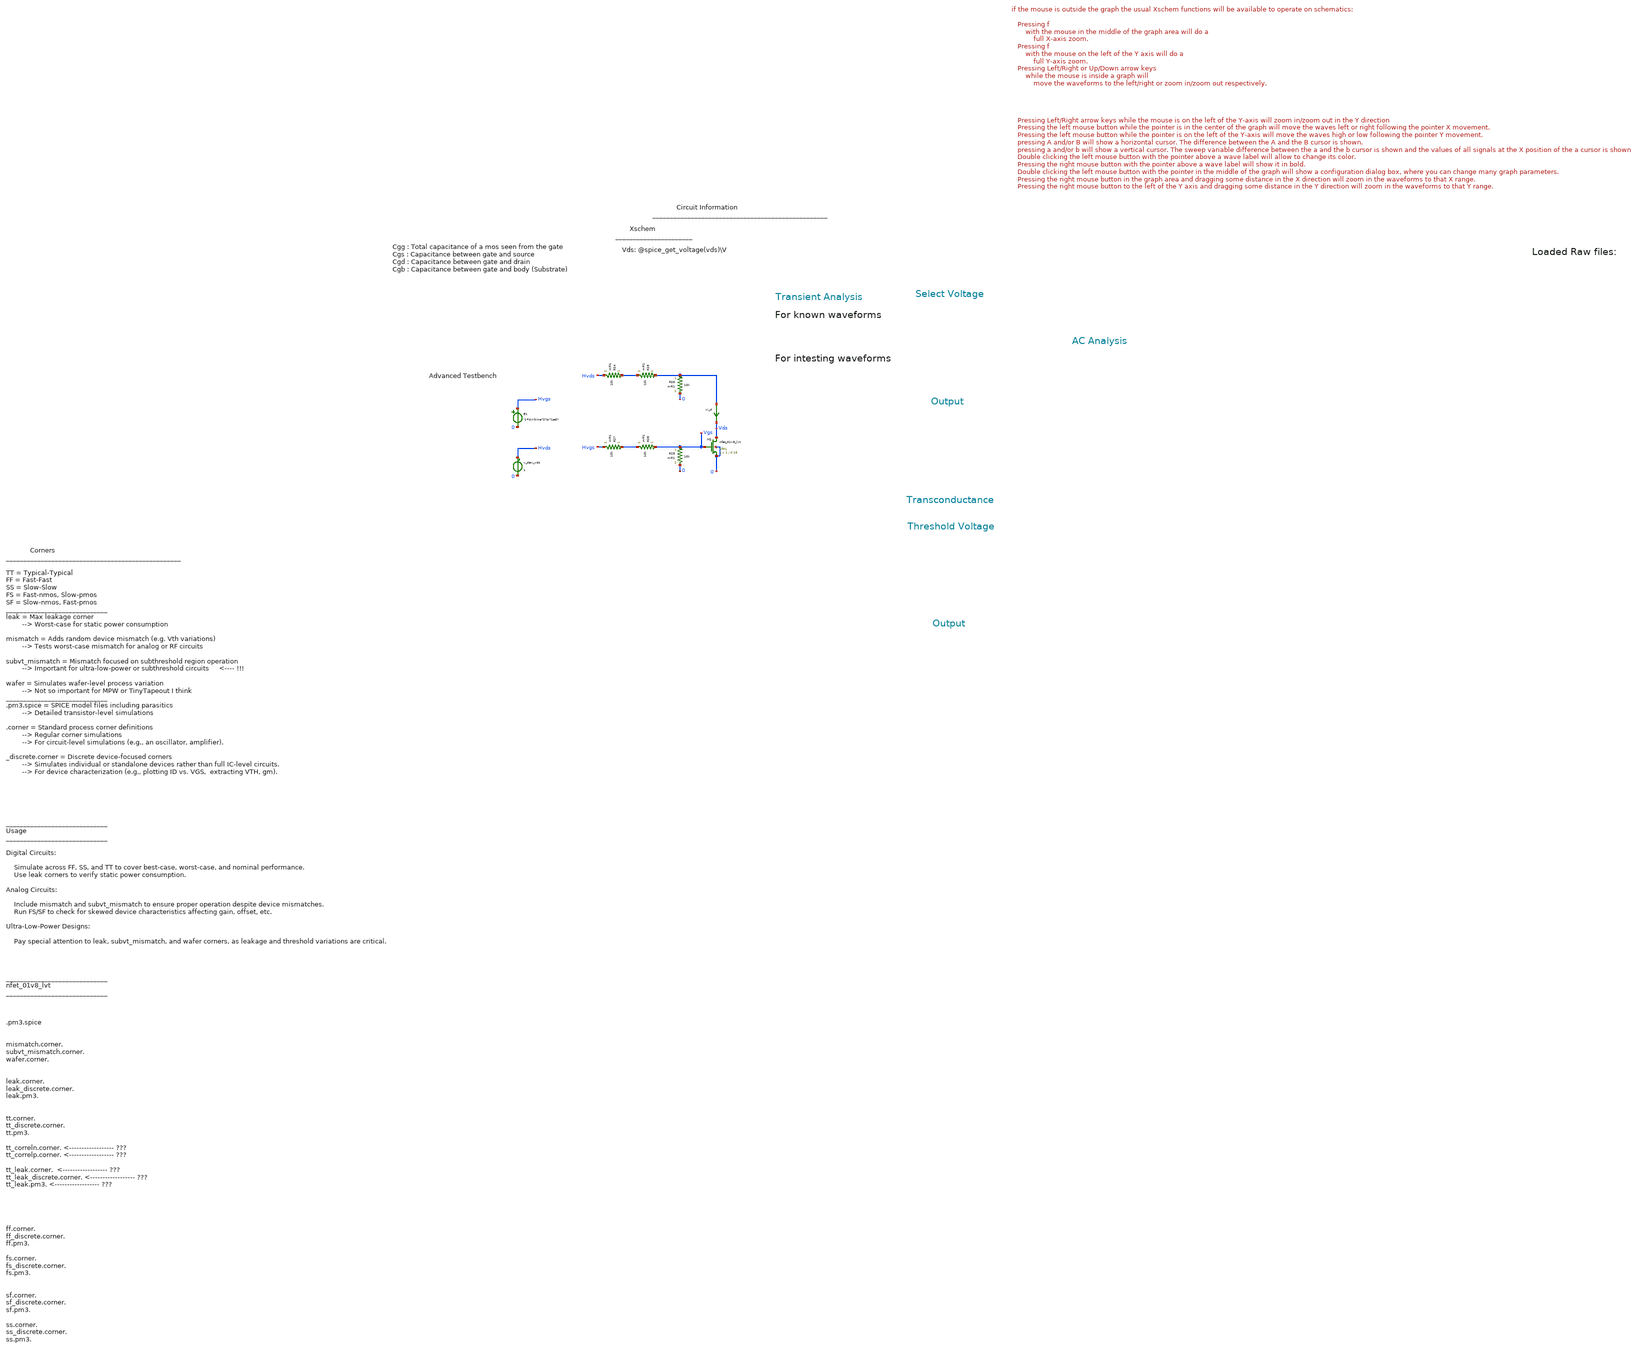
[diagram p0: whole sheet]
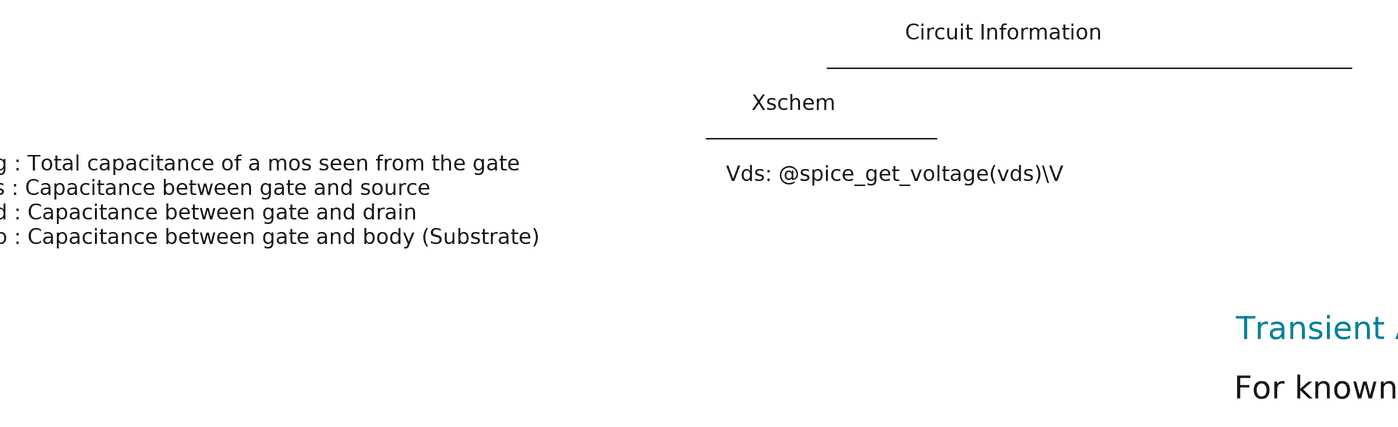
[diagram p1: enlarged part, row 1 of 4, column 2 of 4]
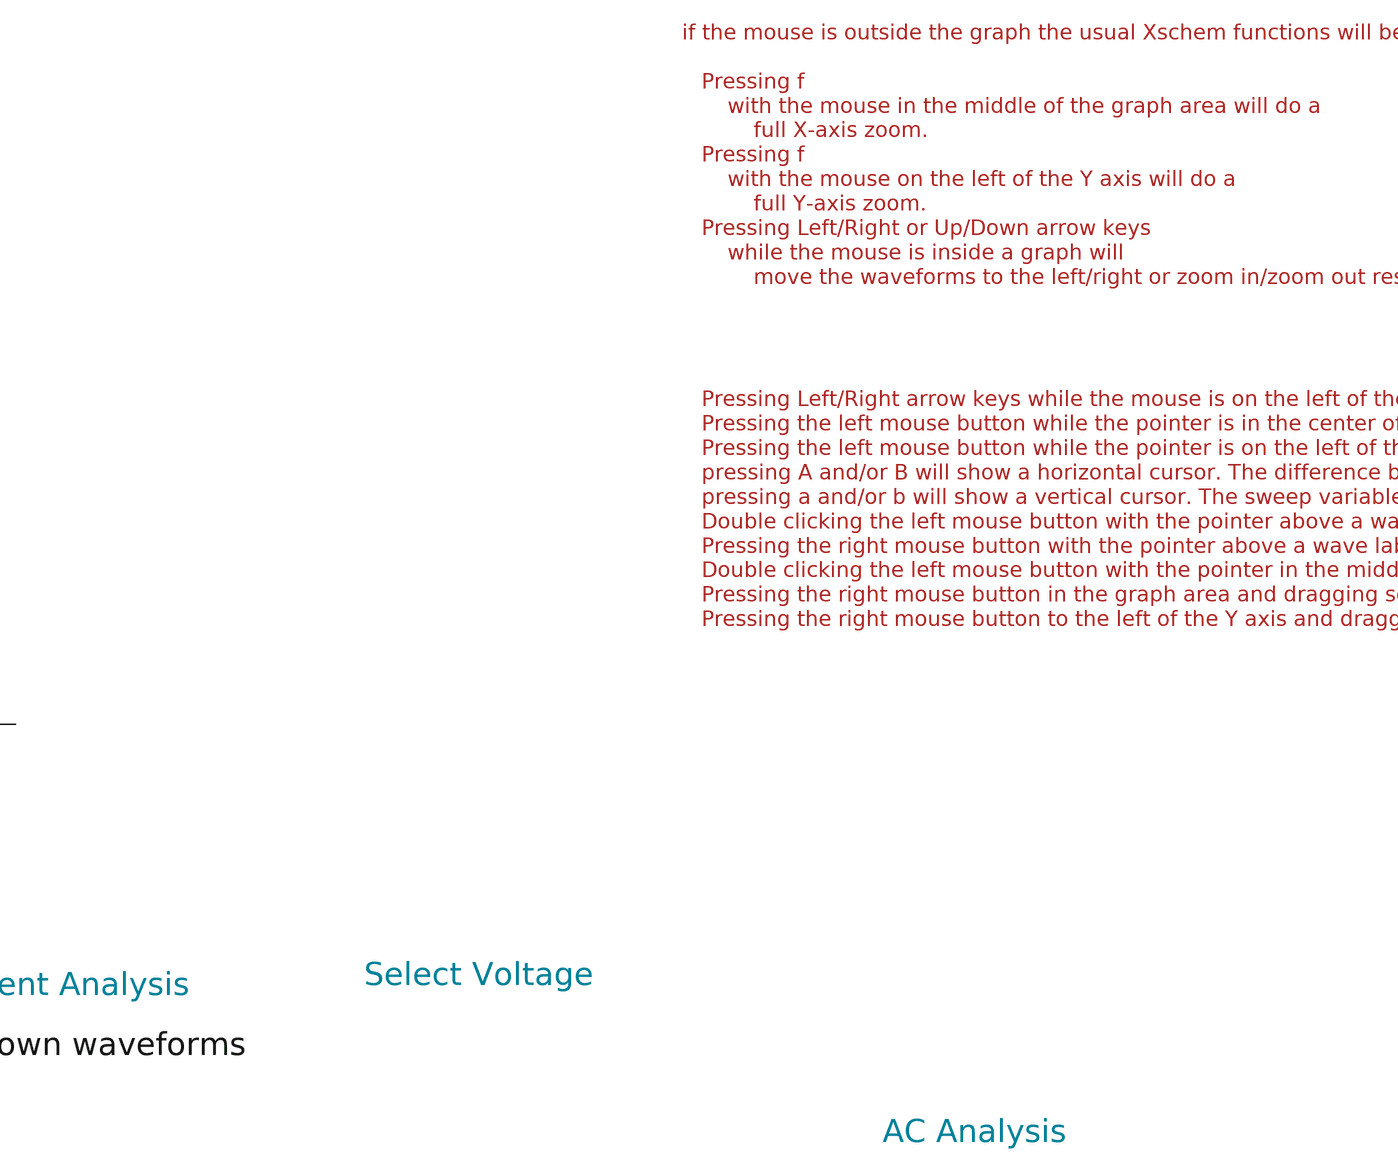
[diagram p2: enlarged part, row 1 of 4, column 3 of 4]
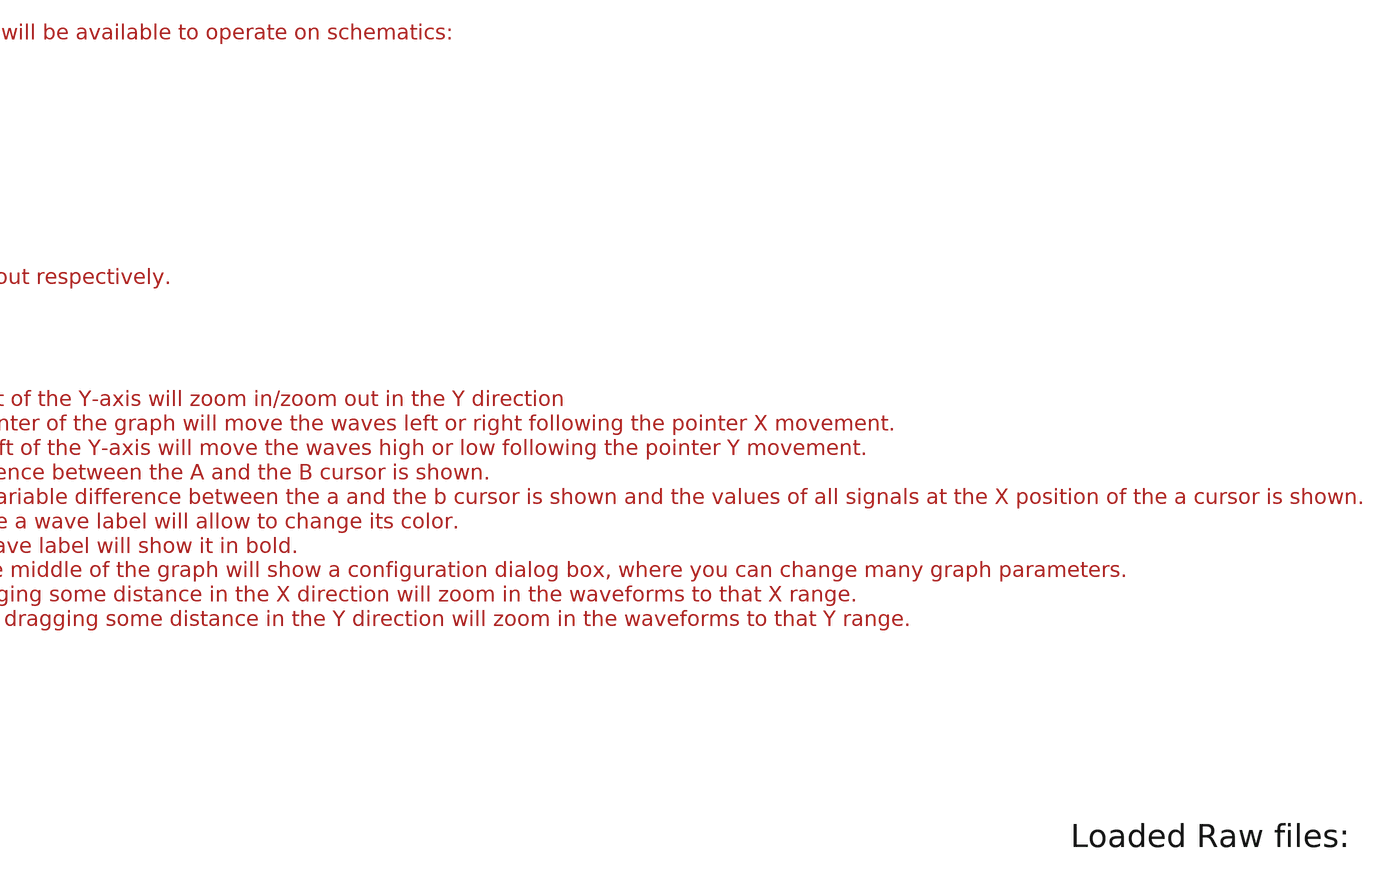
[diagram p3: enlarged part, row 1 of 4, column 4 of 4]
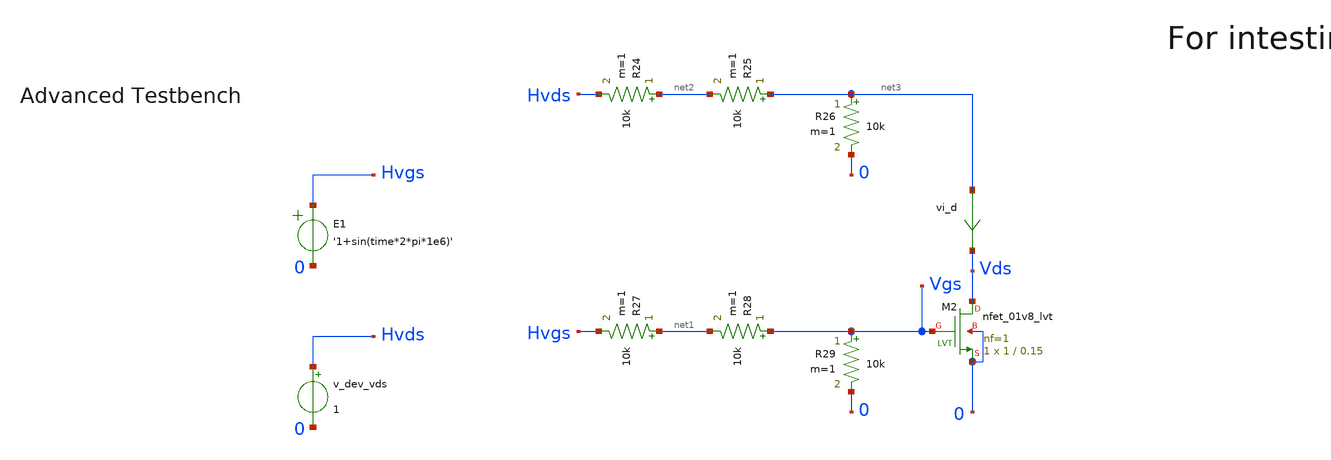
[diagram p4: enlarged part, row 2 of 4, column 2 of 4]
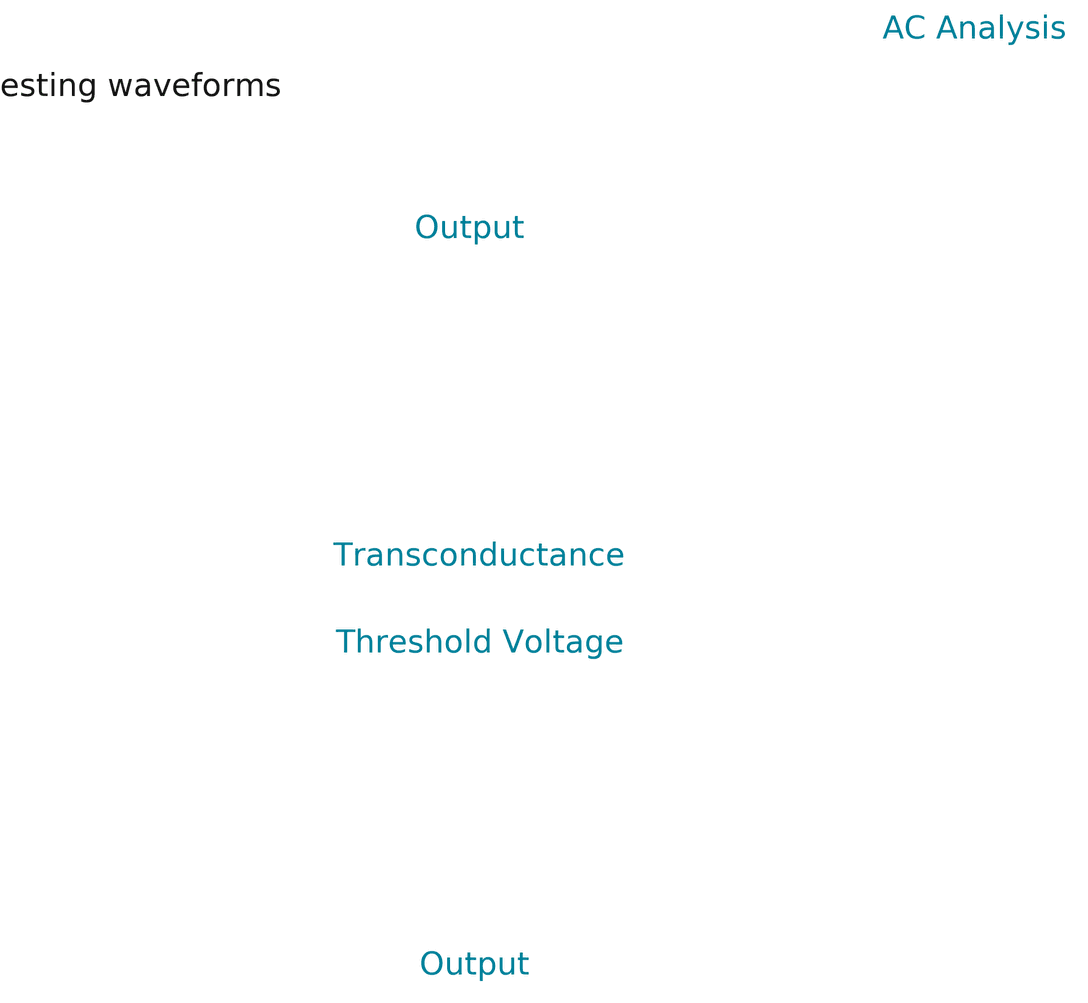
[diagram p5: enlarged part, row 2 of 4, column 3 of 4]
** sch_path: tt10-hdl/tt_um_test_commit/xschem/T0/nmos_tran.sch
* Copyright (C) 1998-2024 Stefan Frederik Schippers
* This program is free software; you can redistribute it and/or modify
* it under the terms of the GNU General Public License as published by
* the Free Software Foundation; either version 2 of the License, or
* (at your option) any later version.
* This program is distributed in the hope that it will be useful,
* but WITHOUT ANY WARRANTY; without even the implied warranty of
* MERCHANTABILITY or FITNESS FOR A PARTICULAR PURPOSE.  See the
* GNU General Public License for more details.
* You should have received a copy of the GNU General Public License
* along with this program; if not, write to the Free Software
**.subckt nmos_tran
vi_d net3 Vds 0
.save i(vi_d)
v_dev_vds Hvds 0 1
E1 Hvgs 0 VOL=' '1+sin(time*2*pi*1e6)' '
R27 net1 Hvgs 10k m=1
R28 Vgs net1 10k m=1
R29 Vgs 0 10k m=1
XM2 Vds Vgs 0 0 sky130_fd_pr__nfet_01v8_lvt L=0.15 W=1 nf=1 ad='int((1 + 1)/2) * 1 / 1 * 0.29' as='int((1 + 2)/2) * 1 / 1 * 0.29'
+ pd='2*int((1 + 1)/2) * (1 / 1 + 0.29)' ps='2*int((1 + 2)/2) * (1 / 1 + 0.29)' nrd='0.29 / 1 ' nrs='0.29 / 1 '
+ sa=0 sb=0 sd=0 mult=1 m=1
R24 net2 Hvds 10k m=1
R25 net3 net2 10k m=1
R26 net3 0 10k m=1
**** begin user architecture code



.temp 30

*.option gmin=5n
*.option scale=1e-6
.option wnflag=1
.option savecurrents

.save all
.control
  save all alli

  save @m.xm1.msky130_fd_pr__nfet_01v8_lvt[gm]
  save @m.xm1.msky130_fd_pr__nfet_01v8_lvt[id]
  save @m.xm1.msky130_fd_pr__nfet_01v8_lvt[vgs]

  save @m.xm1.msky130_fd_pr__nfet_01v8_lvt[cgg]
  save @m.xm1.msky130_fd_pr__nfet_01v8_lvt[cgs]
  save @m.xm1.msky130_fd_pr__nfet_01v8_lvt[cgdo]
  save @m.xm1.msky130_fd_pr__nfet_01v8_lvt[cgb]

  save @m.xm1.msky130_fd_pr__nfet_01v8_lvt[vds]
  save @m.xm1.msky130_fd_pr__nfet_01v8_lvt[vdsat]
  save @m.xm1.msky130_fd_pr__nfet_01v8_lvt[vth]


  save @m.xm1.msky130_fd_pr__nfet_01v8_lvt[leff]
  save @m.xm1.msky130_fd_pr__nfet_01v8_lvt[weff]
  save @m.xm1.msky130_fd_pr__nfet_01v8_lvt[gds]
  save @m.xm1.msky130_fd_pr__nfet_01v8_lvt[l]
  save @m.xm1.msky130_fd_pr__nfet_01v8_lvt[w]
  save @m.xm1.msky130_fd_pr__nfet_01v8_lvt[gm]
  save @m.xm1.msky130_fd_pr__nfet_01v8_lvt[gm]
  save @m.xm1.msky130_fd_pr__nfet_01v8_lvt[gm]
  save @m.xm1.msky130_fd_pr__nfet_01v8_lvt[gm]
  save @m.xm1.msky130_fd_pr__nfet_01v8_lvt[gm]



  *dc v_dev_vds 0 1.8 0.005 v_dev_vgs 0 1.8 0.2
  *write nmos_tb.raw




  tran 1n 5u
  write nmos_tb_tran.raw

  op
  set appendwrite
  write nmos_tb_tran.raw






  *quit 0




.endc





** opencircuitdesign pdks install
.lib $::SKYWATER_MODELS/sky130.lib.spice tt
.include $::SKYWATER_STDCELLS/sky130_fd_sc_hd.spice


**** end user architecture code
**.ends
.end
